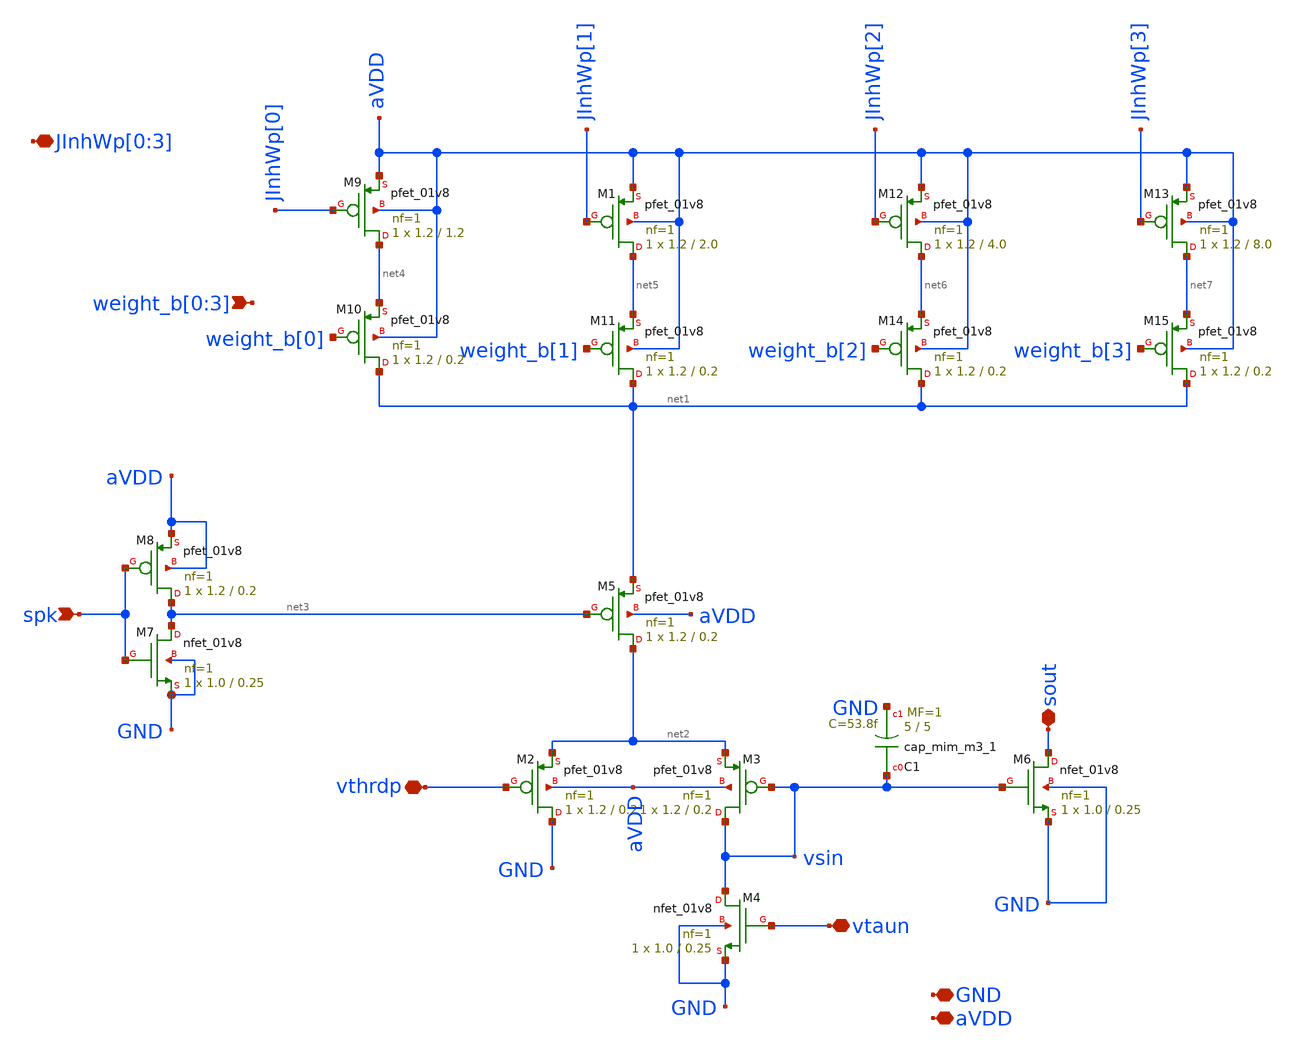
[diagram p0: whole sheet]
** sch_path: design/xschem/dpi_syn_inh_4bit_fc_v2.sch
**.subckt dpi_syn_inh_4bit_fc_v2 spk vthrdp vtaun sout GND aVDD
*+ weight_b[0],weight_b[1],weight_b[2],weight_b[3] JInhWp[0],JInhWp[1],JInhWp[2],JInhWp[3]
*.ipin spk
*.iopin vthrdp
*.iopin vtaun
*.iopin sout
*.iopin GND
*.iopin aVDD
*.ipin weight_b[0],weight_b[1],weight_b[2],weight_b[3]
*.iopin JInhWp[0],JInhWp[1],JInhWp[2],JInhWp[3]
XM5 net2 net3 net1 aVDD sky130_fd_pr__pfet_01v8 L=0.2 W=1.2 nf=1 ad='int((nf+1)/2) * W/nf * 0.29' as='int((nf+2)/2) * W/nf * 0.29'
+ pd='2*int((nf+1)/2) * (W/nf + 0.29)' ps='2*int((nf+2)/2) * (W/nf + 0.29)' nrd='0.29 / W' nrs='0.29 / W'
+ sa=0 sb=0 sd=0 mult=1 m=1
XM2 GND vthrdp net2 aVDD sky130_fd_pr__pfet_01v8 L=0.2 W=1.2 nf=1 ad='int((nf+1)/2) * W/nf * 0.29' as='int((nf+2)/2) * W/nf * 0.29'
+ pd='2*int((nf+1)/2) * (W/nf + 0.29)' ps='2*int((nf+2)/2) * (W/nf + 0.29)' nrd='0.29 / W' nrs='0.29 / W'
+ sa=0 sb=0 sd=0 mult=1 m=1
XM3 vsin vsin net2 aVDD sky130_fd_pr__pfet_01v8 L=0.2 W=1.2 nf=1 ad='int((nf+1)/2) * W/nf * 0.29' as='int((nf+2)/2) * W/nf * 0.29'
+ pd='2*int((nf+1)/2) * (W/nf + 0.29)' ps='2*int((nf+2)/2) * (W/nf + 0.29)' nrd='0.29 / W' nrs='0.29 / W'
+ sa=0 sb=0 sd=0 mult=1 m=1
XM4 vsin vtaun GND GND sky130_fd_pr__nfet_01v8 L=0.25 W=1.0 nf=1 ad='int((nf+1)/2) * W/nf * 0.29' as='int((nf+2)/2) * W/nf * 0.29'
+ pd='2*int((nf+1)/2) * (W/nf + 0.29)' ps='2*int((nf+2)/2) * (W/nf + 0.29)' nrd='0.29 / W' nrs='0.29 / W'
+ sa=0 sb=0 sd=0 mult=1 m=1
XM6 sout vsin GND GND sky130_fd_pr__nfet_01v8 L=0.25 W=1.0 nf=1 ad='int((nf+1)/2) * W/nf * 0.29' as='int((nf+2)/2) * W/nf * 0.29'
+ pd='2*int((nf+1)/2) * (W/nf + 0.29)' ps='2*int((nf+2)/2) * (W/nf + 0.29)' nrd='0.29 / W' nrs='0.29 / W'
+ sa=0 sb=0 sd=0 mult=1 m=1
XM7 net3 spk GND GND sky130_fd_pr__nfet_01v8 L=0.25 W=1.0 nf=1 ad='int((nf+1)/2) * W/nf * 0.29' as='int((nf+2)/2) * W/nf * 0.29'
+ pd='2*int((nf+1)/2) * (W/nf + 0.29)' ps='2*int((nf+2)/2) * (W/nf + 0.29)' nrd='0.29 / W' nrs='0.29 / W'
+ sa=0 sb=0 sd=0 mult=1 m=1
XM8 net3 spk aVDD aVDD sky130_fd_pr__pfet_01v8 L=0.2 W=1.2 nf=1 ad='int((nf+1)/2) * W/nf * 0.29' as='int((nf+2)/2) * W/nf * 0.29'
+ pd='2*int((nf+1)/2) * (W/nf + 0.29)' ps='2*int((nf+2)/2) * (W/nf + 0.29)' nrd='0.29 / W' nrs='0.29 / W'
+ sa=0 sb=0 sd=0 mult=1 m=1
XC1 vsin GND sky130_fd_pr__cap_mim_m3_1 W=5 L=5 MF=1 m=1
XM9 net4 JInhWp[0] aVDD aVDD sky130_fd_pr__pfet_01v8 L=1.2 W=1.2 nf=1 ad='int((nf+1)/2) * W/nf * 0.29'
+ as='int((nf+2)/2) * W/nf * 0.29' pd='2*int((nf+1)/2) * (W/nf + 0.29)' ps='2*int((nf+2)/2) * (W/nf + 0.29)'
+ nrd='0.29 / W' nrs='0.29 / W' sa=0 sb=0 sd=0 mult=1 m=1
XM10 net1 weight_b[0] net4 aVDD sky130_fd_pr__pfet_01v8 L=0.2 W=1.2 nf=1 ad='int((nf+1)/2) * W/nf * 0.29'
+ as='int((nf+2)/2) * W/nf * 0.29' pd='2*int((nf+1)/2) * (W/nf + 0.29)' ps='2*int((nf+2)/2) * (W/nf + 0.29)'
+ nrd='0.29 / W' nrs='0.29 / W' sa=0 sb=0 sd=0 mult=1 m=1
XM11 net1 weight_b[1] net5 aVDD sky130_fd_pr__pfet_01v8 L=0.2 W=1.2 nf=1 ad='int((nf+1)/2) * W/nf * 0.29'
+ as='int((nf+2)/2) * W/nf * 0.29' pd='2*int((nf+1)/2) * (W/nf + 0.29)' ps='2*int((nf+2)/2) * (W/nf + 0.29)'
+ nrd='0.29 / W' nrs='0.29 / W' sa=0 sb=0 sd=0 mult=1 m=1
XM1 net5 JInhWp[1] aVDD aVDD sky130_fd_pr__pfet_01v8 L=2.0 W=1.2 nf=1 ad='int((nf+1)/2) * W/nf * 0.29'
+ as='int((nf+2)/2) * W/nf * 0.29' pd='2*int((nf+1)/2) * (W/nf + 0.29)' ps='2*int((nf+2)/2) * (W/nf + 0.29)'
+ nrd='0.29 / W' nrs='0.29 / W' sa=0 sb=0 sd=0 mult=1 m=1
XM12 net6 JInhWp[2] aVDD aVDD sky130_fd_pr__pfet_01v8 L=4.0 W=1.2 nf=1 ad='int((nf+1)/2) * W/nf * 0.29'
+ as='int((nf+2)/2) * W/nf * 0.29' pd='2*int((nf+1)/2) * (W/nf + 0.29)' ps='2*int((nf+2)/2) * (W/nf + 0.29)'
+ nrd='0.29 / W' nrs='0.29 / W' sa=0 sb=0 sd=0 mult=1 m=1
XM13 net7 JInhWp[3] aVDD aVDD sky130_fd_pr__pfet_01v8 L=8.0 W=1.2 nf=1 ad='int((nf+1)/2) * W/nf * 0.29'
+ as='int((nf+2)/2) * W/nf * 0.29' pd='2*int((nf+1)/2) * (W/nf + 0.29)' ps='2*int((nf+2)/2) * (W/nf + 0.29)'
+ nrd='0.29 / W' nrs='0.29 / W' sa=0 sb=0 sd=0 mult=1 m=1
XM14 net1 weight_b[2] net6 aVDD sky130_fd_pr__pfet_01v8 L=0.2 W=1.2 nf=1 ad='int((nf+1)/2) * W/nf * 0.29'
+ as='int((nf+2)/2) * W/nf * 0.29' pd='2*int((nf+1)/2) * (W/nf + 0.29)' ps='2*int((nf+2)/2) * (W/nf + 0.29)'
+ nrd='0.29 / W' nrs='0.29 / W' sa=0 sb=0 sd=0 mult=1 m=1
XM15 net1 weight_b[3] net7 aVDD sky130_fd_pr__pfet_01v8 L=0.2 W=1.2 nf=1 ad='int((nf+1)/2) * W/nf * 0.29'
+ as='int((nf+2)/2) * W/nf * 0.29' pd='2*int((nf+1)/2) * (W/nf + 0.29)' ps='2*int((nf+2)/2) * (W/nf + 0.29)'
+ nrd='0.29 / W' nrs='0.29 / W' sa=0 sb=0 sd=0 mult=1 m=1
**.ends
.end
